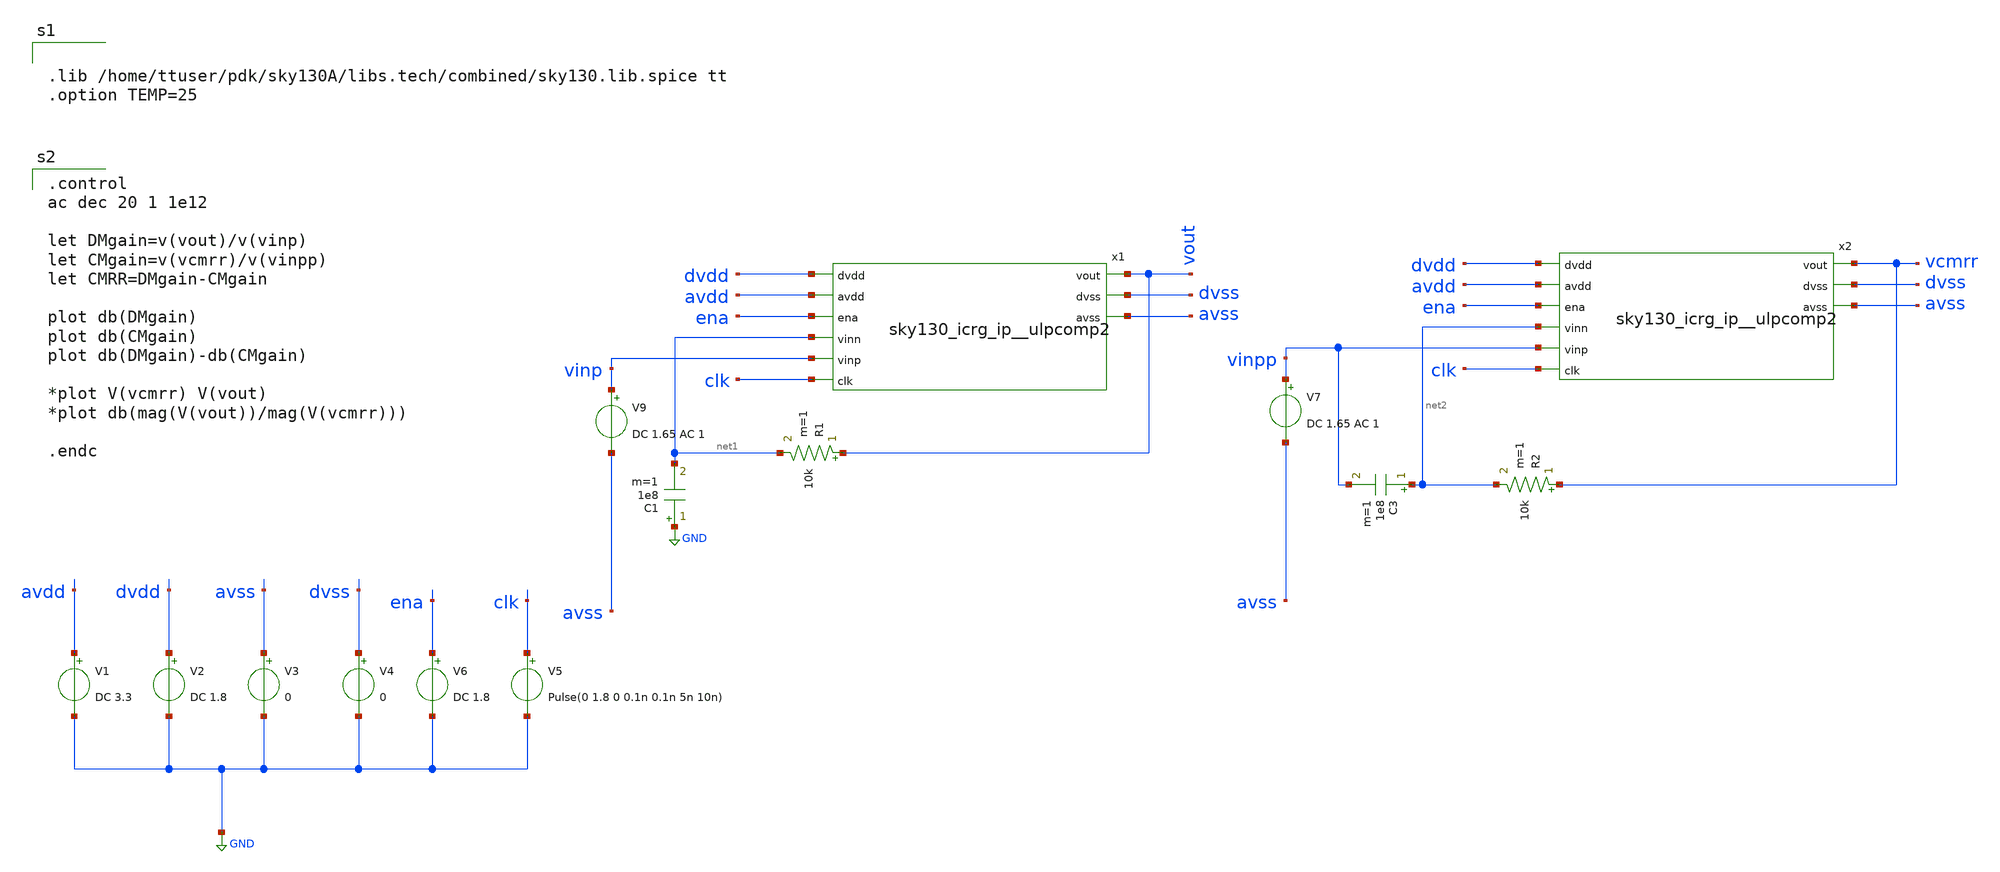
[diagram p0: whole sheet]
** sch_path: xschem/CMRR_tb.sch
**.subckt CMRR_tb
x1 dvdd avdd ena vout net1 vinp clk dvss avss sky130_icrg_ip__ulpcomp2
V1 avdd GND DC 3.3
V2 dvdd GND DC 1.8
V3 avss GND 0
V4 dvss GND 0
V5 clk GND Pulse(0 1.8 0 0.1n 0.1n 5n 10n)
V6 ena GND DC 1.8
V9 vinp avss DC 1.65 AC 1
x2 dvdd avdd ena vcmrr net2 vinpp clk dvss avss sky130_icrg_ip__ulpcomp2
R2 vcmrr net2 10k m=1
C3 net2 vinpp 1e8 m=1
V7 vinpp avss DC 1.65 AC 1
R1 vout net1 10k m=1
C1 GND net1 1e8 m=1
**** begin user architecture code


.lib /home/ttuser/pdk/sky130A/libs.tech/combined/sky130.lib.spice tt
.option TEMP=25


.control
ac dec 20 1 1e12

let DMgain=v(vout)/v(vinp)
let CMgain=v(vcmrr)/v(vinpp)
let CMRR=DMgain-CMgain

plot db(DMgain)
plot db(CMgain)
plot db(DMgain)-db(CMgain)

*plot V(vcmrr) V(vout)
*plot db(mag(V(vout))/mag(V(vcmrr)))

.endc

**** end user architecture code
**.ends

* expanding   symbol:  sky130_icrg_ip__ulpcomp2.sym # of pins=9
** sym_path: xschem/sky130_icrg_ip__ulpcomp2.sym
** sch_path: xschem/sky130_icrg_ip__ulpcomp2.sch
.subckt sky130_icrg_ip__ulpcomp2 dvdd avdd ena vout vinn vinp clk dvss avss
*.ipin avdd
*.ipin vinp
*.ipin vinn
*.opin avss
*.opin vout
*.opin dvss
*.ipin dvdd
*.ipin clk
*.ipin ena
XM2 oneg vinp net1 net1 sky130_fd_pr__pfet_g5v0d10v5 L=1 W=5 nf=1 ad='int((nf+1)/2) * W/nf * 0.29' as='int((nf+2)/2) * W/nf * 0.29'
+ pd='2*int((nf+1)/2) * (W/nf + 0.29)' ps='2*int((nf+2)/2) * (W/nf + 0.29)' nrd='0.29 / W' nrs='0.29 / W'
+ sa=0 sb=0 sd=0 mult=1 m=1
XM3 opos vinn net1 net1 sky130_fd_pr__pfet_g5v0d10v5 L=1 W=5 nf=1 ad='int((nf+1)/2) * W/nf * 0.29' as='int((nf+2)/2) * W/nf * 0.29'
+ pd='2*int((nf+1)/2) * (W/nf + 0.29)' ps='2*int((nf+2)/2) * (W/nf + 0.29)' nrd='0.29 / W' nrs='0.29 / W'
+ sa=0 sb=0 sd=0 mult=1 m=1
XM7 oneg clka net2 net2 sky130_fd_pr__nfet_03v3_nvt L=0.5 W=3 nf=1 ad='int((nf+1)/2) * W/nf * 0.29' as='int((nf+2)/2) * W/nf * 0.29'
+ pd='2*int((nf+1)/2) * (W/nf + 0.29)' ps='2*int((nf+2)/2) * (W/nf + 0.29)' nrd='0.29 / W' nrs='0.29 / W'
+ sa=0 sb=0 sd=0 mult=1 m=1
XM5 opos clka net2 net2 sky130_fd_pr__nfet_03v3_nvt L=0.5 W=3 nf=1 ad='int((nf+1)/2) * W/nf * 0.29' as='int((nf+2)/2) * W/nf * 0.29'
+ pd='2*int((nf+1)/2) * (W/nf + 0.29)' ps='2*int((nf+2)/2) * (W/nf + 0.29)' nrd='0.29 / W' nrs='0.29 / W'
+ sa=0 sb=0 sd=0 mult=1 m=1
XM4 net2 net2 avss avss sky130_fd_pr__nfet_03v3_nvt L=0.5 W=3 nf=1 ad='int((nf+1)/2) * W/nf * 0.29' as='int((nf+2)/2) * W/nf * 0.29'
+ pd='2*int((nf+1)/2) * (W/nf + 0.29)' ps='2*int((nf+2)/2) * (W/nf + 0.29)' nrd='0.29 / W' nrs='0.29 / W'
+ sa=0 sb=0 sd=0 mult=1 m=1
XM18 vout net4 dvss dvss sky130_fd_pr__nfet_01v8 L=0.5 W=1 nf=1 ad='int((nf+1)/2) * W/nf * 0.29' as='int((nf+2)/2) * W/nf * 0.29'
+ pd='2*int((nf+1)/2) * (W/nf + 0.29)' ps='2*int((nf+2)/2) * (W/nf + 0.29)' nrd='0.29 / W' nrs='0.29 / W'
+ sa=0 sb=0 sd=0 mult=1 m=1
XM19 vout net4 dvddb dvddb sky130_fd_pr__pfet_01v8 L=1 W=2 nf=1 ad='int((nf+1)/2) * W/nf * 0.29' as='int((nf+2)/2) * W/nf * 0.29'
+ pd='2*int((nf+1)/2) * (W/nf + 0.29)' ps='2*int((nf+2)/2) * (W/nf + 0.29)' nrd='0.29 / W' nrs='0.29 / W'
+ sa=0 sb=0 sd=0 mult=1 m=1
XM22 clka clkb dvddb dvddb sky130_fd_pr__pfet_01v8 L=0.5 W=2 nf=1 ad='int((nf+1)/2) * W/nf * 0.29' as='int((nf+2)/2) * W/nf * 0.29'
+ pd='2*int((nf+1)/2) * (W/nf + 0.29)' ps='2*int((nf+2)/2) * (W/nf + 0.29)' nrd='0.29 / W' nrs='0.29 / W'
+ sa=0 sb=0 sd=0 mult=1 m=1
XM20 net3 enab avdd avdd sky130_fd_pr__pfet_g5v0d10v5 L=1 W=5 nf=1 ad='int((nf+1)/2) * W/nf * 0.29' as='int((nf+2)/2) * W/nf * 0.29'
+ pd='2*int((nf+1)/2) * (W/nf + 0.29)' ps='2*int((nf+2)/2) * (W/nf + 0.29)' nrd='0.29 / W' nrs='0.29 / W'
+ sa=0 sb=0 sd=0 mult=1 m=1
XM8 clkb clk dvddb dvddb sky130_fd_pr__pfet_01v8 L=0.5 W=2 nf=1 ad='int((nf+1)/2) * W/nf * 0.29' as='int((nf+2)/2) * W/nf * 0.29'
+ pd='2*int((nf+1)/2) * (W/nf + 0.29)' ps='2*int((nf+2)/2) * (W/nf + 0.29)' nrd='0.29 / W' nrs='0.29 / W'
+ sa=0 sb=0 sd=0 mult=1 m=1
XM25 enab ena dvdd dvdd sky130_fd_pr__pfet_01v8 L=0.5 W=2 nf=1 ad='int((nf+1)/2) * W/nf * 0.29' as='int((nf+2)/2) * W/nf * 0.29'
+ pd='2*int((nf+1)/2) * (W/nf + 0.29)' ps='2*int((nf+2)/2) * (W/nf + 0.29)' nrd='0.29 / W' nrs='0.29 / W'
+ sa=0 sb=0 sd=0 mult=1 m=1
XM13 net4 opos net6 dvss sky130_fd_pr__nfet_03v3_nvt L=0.5 W=2 nf=1 ad='int((nf+1)/2) * W/nf * 0.29'
+ as='int((nf+2)/2) * W/nf * 0.29' pd='2*int((nf+1)/2) * (W/nf + 0.29)' ps='2*int((nf+2)/2) * (W/nf + 0.29)'
+ nrd='0.29 / W' nrs='0.29 / W' sa=0 sb=0 sd=0 mult=1 m=1
XM14 net7 net4 net8 dvss sky130_fd_pr__nfet_03v3_nvt L=0.5 W=2 nf=1 ad='int((nf+1)/2) * W/nf * 0.29'
+ as='int((nf+2)/2) * W/nf * 0.29' pd='2*int((nf+1)/2) * (W/nf + 0.29)' ps='2*int((nf+2)/2) * (W/nf + 0.29)'
+ nrd='0.29 / W' nrs='0.29 / W' sa=0 sb=0 sd=0 mult=1 m=1
XM15 net8 clkb dvss dvss sky130_fd_pr__nfet_03v3_nvt L=0.5 W=2 nf=1 ad='int((nf+1)/2) * W/nf * 0.29'
+ as='int((nf+2)/2) * W/nf * 0.29' pd='2*int((nf+1)/2) * (W/nf + 0.29)' ps='2*int((nf+2)/2) * (W/nf + 0.29)'
+ nrd='0.29 / W' nrs='0.29 / W' sa=0 sb=0 sd=0 mult=1 m=1
XM16 net6 net5 net8 dvss sky130_fd_pr__nfet_03v3_nvt L=0.5 W=2 nf=1 ad='int((nf+1)/2) * W/nf * 0.29'
+ as='int((nf+2)/2) * W/nf * 0.29' pd='2*int((nf+1)/2) * (W/nf + 0.29)' ps='2*int((nf+2)/2) * (W/nf + 0.29)'
+ nrd='0.29 / W' nrs='0.29 / W' sa=0 sb=0 sd=0 mult=1 m=1
XM17 net5 oneg net7 dvss sky130_fd_pr__nfet_03v3_nvt L=0.5 W=2 nf=1 ad='int((nf+1)/2) * W/nf * 0.29'
+ as='int((nf+2)/2) * W/nf * 0.29' pd='2*int((nf+1)/2) * (W/nf + 0.29)' ps='2*int((nf+2)/2) * (W/nf + 0.29)'
+ nrd='0.29 / W' nrs='0.29 / W' sa=0 sb=0 sd=0 mult=1 m=1
XM6 clkb clk dvss dvss sky130_fd_pr__nfet_01v8 L=0.5 W=1 nf=1 ad='int((nf+1)/2) * W/nf * 0.29' as='int((nf+2)/2) * W/nf * 0.29'
+ pd='2*int((nf+1)/2) * (W/nf + 0.29)' ps='2*int((nf+2)/2) * (W/nf + 0.29)' nrd='0.29 / W' nrs='0.29 / W'
+ sa=0 sb=0 sd=0 mult=1 m=1
XM21 clka clkb dvss dvss sky130_fd_pr__nfet_01v8 L=0.5 W=1 nf=1 ad='int((nf+1)/2) * W/nf * 0.29' as='int((nf+2)/2) * W/nf * 0.29'
+ pd='2*int((nf+1)/2) * (W/nf + 0.29)' ps='2*int((nf+2)/2) * (W/nf + 0.29)' nrd='0.29 / W' nrs='0.29 / W'
+ sa=0 sb=0 sd=0 mult=1 m=1
XM24 enab ena dvss dvss sky130_fd_pr__nfet_01v8 L=0.5 W=1 nf=1 ad='int((nf+1)/2) * W/nf * 0.29' as='int((nf+2)/2) * W/nf * 0.29'
+ pd='2*int((nf+1)/2) * (W/nf + 0.29)' ps='2*int((nf+2)/2) * (W/nf + 0.29)' nrd='0.29 / W' nrs='0.29 / W'
+ sa=0 sb=0 sd=0 mult=1 m=1
XM1 net1 clka net3 net3 sky130_fd_pr__pfet_g5v0d10v5 L=1 W=5 nf=1 ad='int((nf+1)/2) * W/nf * 0.29' as='int((nf+2)/2) * W/nf * 0.29'
+ pd='2*int((nf+1)/2) * (W/nf + 0.29)' ps='2*int((nf+2)/2) * (W/nf + 0.29)' nrd='0.29 / W' nrs='0.29 / W'
+ sa=0 sb=0 sd=0 mult=1 m=1
XM23 dvddb enab dvdd dvdd sky130_fd_pr__pfet_01v8_hvt L=0.15 W=1 nf=1 ad='int((nf+1)/2) * W/nf * 0.29'
+ as='int((nf+2)/2) * W/nf * 0.29' pd='2*int((nf+1)/2) * (W/nf + 0.29)' ps='2*int((nf+2)/2) * (W/nf + 0.29)'
+ nrd='0.29 / W' nrs='0.29 / W' sa=0 sb=0 sd=0 mult=1 m=1
XM9 net4 clkb dvddb dvddb sky130_fd_pr__pfet_01v8_hvt L=1 W=3 nf=1 ad='int((nf+1)/2) * W/nf * 0.29' as='int((nf+2)/2) * W/nf * 0.29'
+ pd='2*int((nf+1)/2) * (W/nf + 0.29)' ps='2*int((nf+2)/2) * (W/nf + 0.29)' nrd='0.29 / W' nrs='0.29 / W'
+ sa=0 sb=0 sd=0 mult=2 m=2
XM10 net5 net4 dvddb dvddb sky130_fd_pr__pfet_01v8_hvt L=1 W=3 nf=1 ad='int((nf+1)/2) * W/nf * 0.29'
+ as='int((nf+2)/2) * W/nf * 0.29' pd='2*int((nf+1)/2) * (W/nf + 0.29)' ps='2*int((nf+2)/2) * (W/nf + 0.29)'
+ nrd='0.29 / W' nrs='0.29 / W' sa=0 sb=0 sd=0 mult=2 m=2
XM11 net4 net5 dvddb dvddb sky130_fd_pr__pfet_01v8_hvt L=1 W=3 nf=1 ad='int((nf+1)/2) * W/nf * 0.29'
+ as='int((nf+2)/2) * W/nf * 0.29' pd='2*int((nf+1)/2) * (W/nf + 0.29)' ps='2*int((nf+2)/2) * (W/nf + 0.29)'
+ nrd='0.29 / W' nrs='0.29 / W' sa=0 sb=0 sd=0 mult=2 m=2
XM12 net5 clkb dvddb dvddb sky130_fd_pr__pfet_01v8_hvt L=1 W=3 nf=1 ad='int((nf+1)/2) * W/nf * 0.29'
+ as='int((nf+2)/2) * W/nf * 0.29' pd='2*int((nf+1)/2) * (W/nf + 0.29)' ps='2*int((nf+2)/2) * (W/nf + 0.29)'
+ nrd='0.29 / W' nrs='0.29 / W' sa=0 sb=0 sd=0 mult=2 m=2
.ends

.GLOBAL GND
.end
